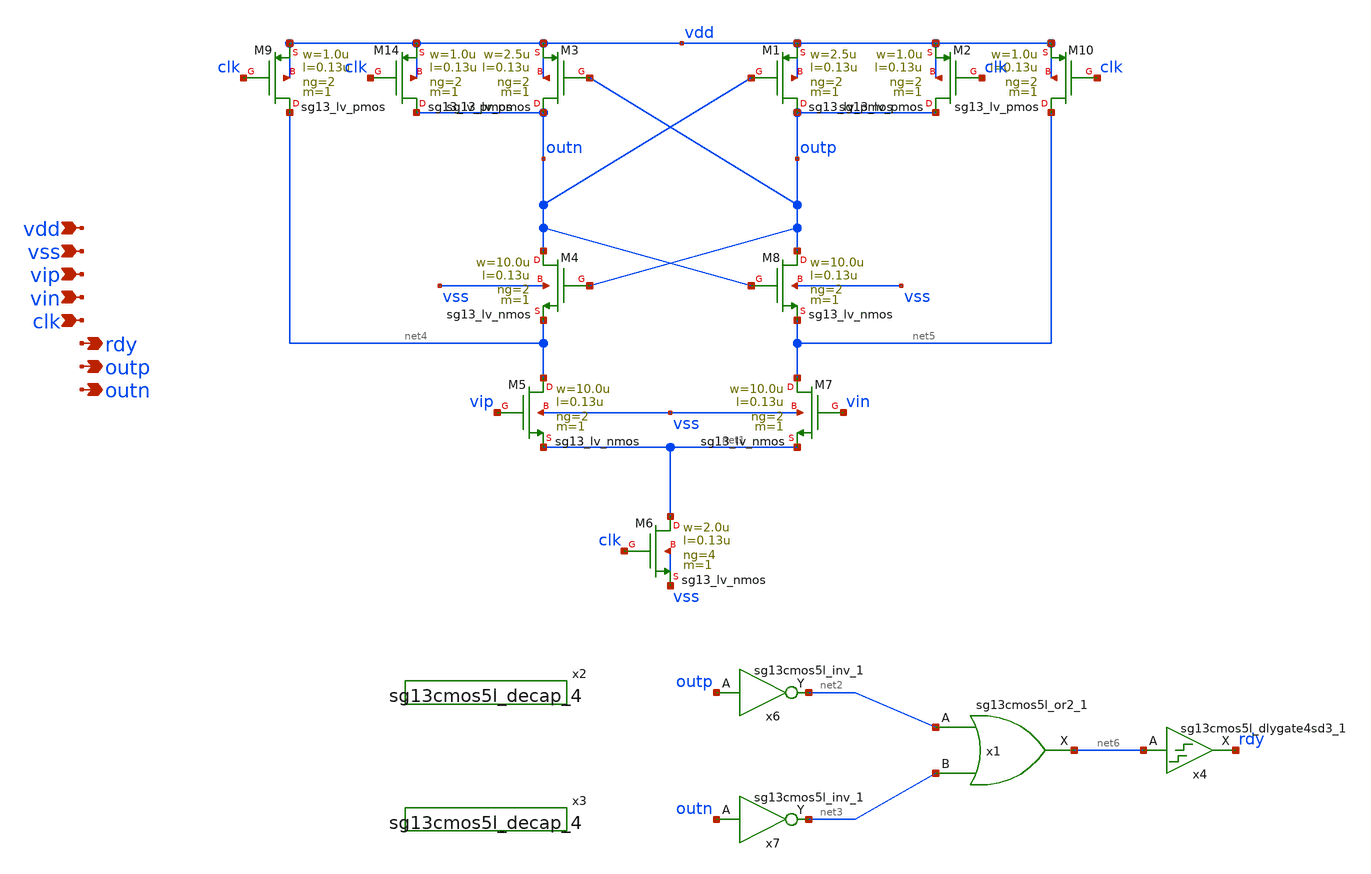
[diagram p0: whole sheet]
** sch_path: MSPHY9932-main/sch/cmp.sch
**.subckt cmp vdd vss vip vin clk rdy outp outn
*.ipin vdd
*.ipin vss
*.ipin vip
*.ipin vin
*.ipin clk
*.opin rdy
*.opin outp
*.opin outn
XM14 outn clk vdd vdd sg13_lv_pmos w=1.0u l=0.13u ng=2 m=1 mm_ok=1
XM1 outp outn vdd vdd sg13_lv_pmos w=2.5u l=0.13u ng=2 m=1 mm_ok=1
XM2 outp clk vdd vdd sg13_lv_pmos w=1.0u l=0.13u ng=2 m=1 mm_ok=1
XM3 outn outp vdd vdd sg13_lv_pmos w=2.5u l=0.13u ng=2 m=1 mm_ok=1
XM5 net4 vip net1 vss sg13_lv_nmos w=10.0u l=0.13u ng=2 m=1 mm_ok=1
XM6 net1 clk vss vss sg13_lv_nmos w=2.0u l=0.13u ng=4 m=1 mm_ok=1
XM7 net5 vin net1 vss sg13_lv_nmos w=10.0u l=0.13u ng=2 m=1 mm_ok=1
x1 net6 net2 net3 vdd vss sg13cmos5l_or2_1
XM4 outn outp net4 vss sg13_lv_nmos w=10.0u l=0.13u ng=2 m=1 mm_ok=1
XM8 outp outn net5 vss sg13_lv_nmos w=10.0u l=0.13u ng=2 m=1 mm_ok=1
XM9 net4 clk vdd vdd sg13_lv_pmos w=1.0u l=0.13u ng=2 m=1 mm_ok=1
XM10 net5 clk vdd vdd sg13_lv_pmos w=1.0u l=0.13u ng=2 m=1 mm_ok=1
x6 net2 outp vdd vss sg13cmos5l_inv_1
x7 net3 outn vdd vss sg13cmos5l_inv_1
x2 vdd vss sg13cmos5l_decap_4
x3 vdd vss sg13cmos5l_decap_4
x4 rdy net6 vdd vss sg13cmos5l_dlygate4sd3_1
**.ends
.end
